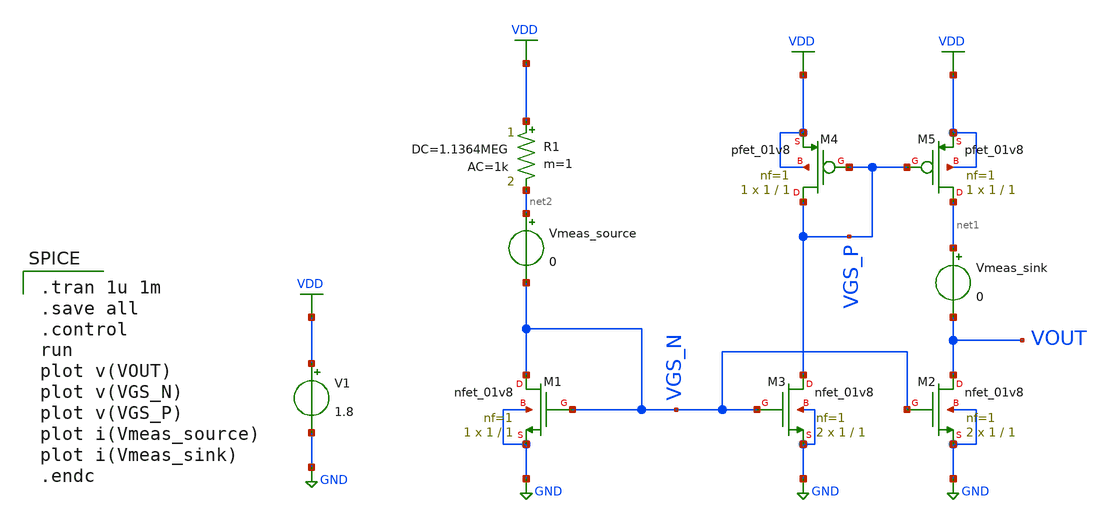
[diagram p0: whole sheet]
** sch_path: Circuits/Examples/Analog/Current_mirror/ActiveLoad_CURRMIRR.sch
**.subckt ActiveLoad_CURRMIRR
V1 VDD GND 1.8
XM1 VGS_N VGS_N GND GND sky130_fd_pr__nfet_01v8 L=1 W=1 nf=1 ad='int((nf+1)/2) * W/nf * 0.29' as='int((nf+2)/2) * W/nf * 0.29'
+ pd='2*int((nf+1)/2) * (W/nf + 0.29)' ps='2*int((nf+2)/2) * (W/nf + 0.29)' nrd='0.29 / W' nrs='0.29 / W'
+ sa=0 sb=0 sd=0 mult=1 m=1
XM2 VOUT VGS_N GND GND sky130_fd_pr__nfet_01v8 L=1 W=1 nf=1 ad='int((nf+1)/2) * W/nf * 0.29' as='int((nf+2)/2) * W/nf * 0.29'
+ pd='2*int((nf+1)/2) * (W/nf + 0.29)' ps='2*int((nf+2)/2) * (W/nf + 0.29)' nrd='0.29 / W' nrs='0.29 / W'
+ sa=0 sb=0 sd=0 mult=2 m=2
Vmeas_sink net1 VOUT 0
XM3 VGS_P VGS_N GND GND sky130_fd_pr__nfet_01v8 L=1 W=1 nf=1 ad='int((nf+1)/2) * W/nf * 0.29' as='int((nf+2)/2) * W/nf * 0.29'
+ pd='2*int((nf+1)/2) * (W/nf + 0.29)' ps='2*int((nf+2)/2) * (W/nf + 0.29)' nrd='0.29 / W' nrs='0.29 / W'
+ sa=0 sb=0 sd=0 mult=2 m=2
XM4 VGS_P VGS_P VDD VDD sky130_fd_pr__pfet_01v8 L=1 W=1 nf=1 ad='int((nf+1)/2) * W/nf * 0.29' as='int((nf+2)/2) * W/nf * 0.29'
+ pd='2*int((nf+1)/2) * (W/nf + 0.29)' ps='2*int((nf+2)/2) * (W/nf + 0.29)' nrd='0.29 / W' nrs='0.29 / W'
+ sa=0 sb=0 sd=0 mult=1 m=1
XM5 net1 VGS_P VDD VDD sky130_fd_pr__pfet_01v8 L=1 W=1 nf=1 ad='int((nf+1)/2) * W/nf * 0.29' as='int((nf+2)/2) * W/nf * 0.29'
+ pd='2*int((nf+1)/2) * (W/nf + 0.29)' ps='2*int((nf+2)/2) * (W/nf + 0.29)' nrd='0.29 / W' nrs='0.29 / W'
+ sa=0 sb=0 sd=0 mult=1 m=1
R1 VDD net2 1.1364MEG ac=1k m=1
Vmeas_source net2 VGS_N 0
**** begin user architecture code
 ** manual skywater pdks install (with patches applied)
* .lib $::SKYWATER_MODELS/models/sky130.lib.spice tt

** opencircuitdesign pdks install
.lib $::SKYWATER_MODELS/sky130.lib.spice tt

.param mc_mm_switch=0
.param mc_pr_switch=0


.tran 1u 1m
.save all
.control
run
plot v(VOUT)
plot v(VGS_N)
plot v(VGS_P)
plot i(Vmeas_source)
plot i(Vmeas_sink)
.endc


**** end user architecture code
**.ends
.GLOBAL GND
.GLOBAL VDD
.end
